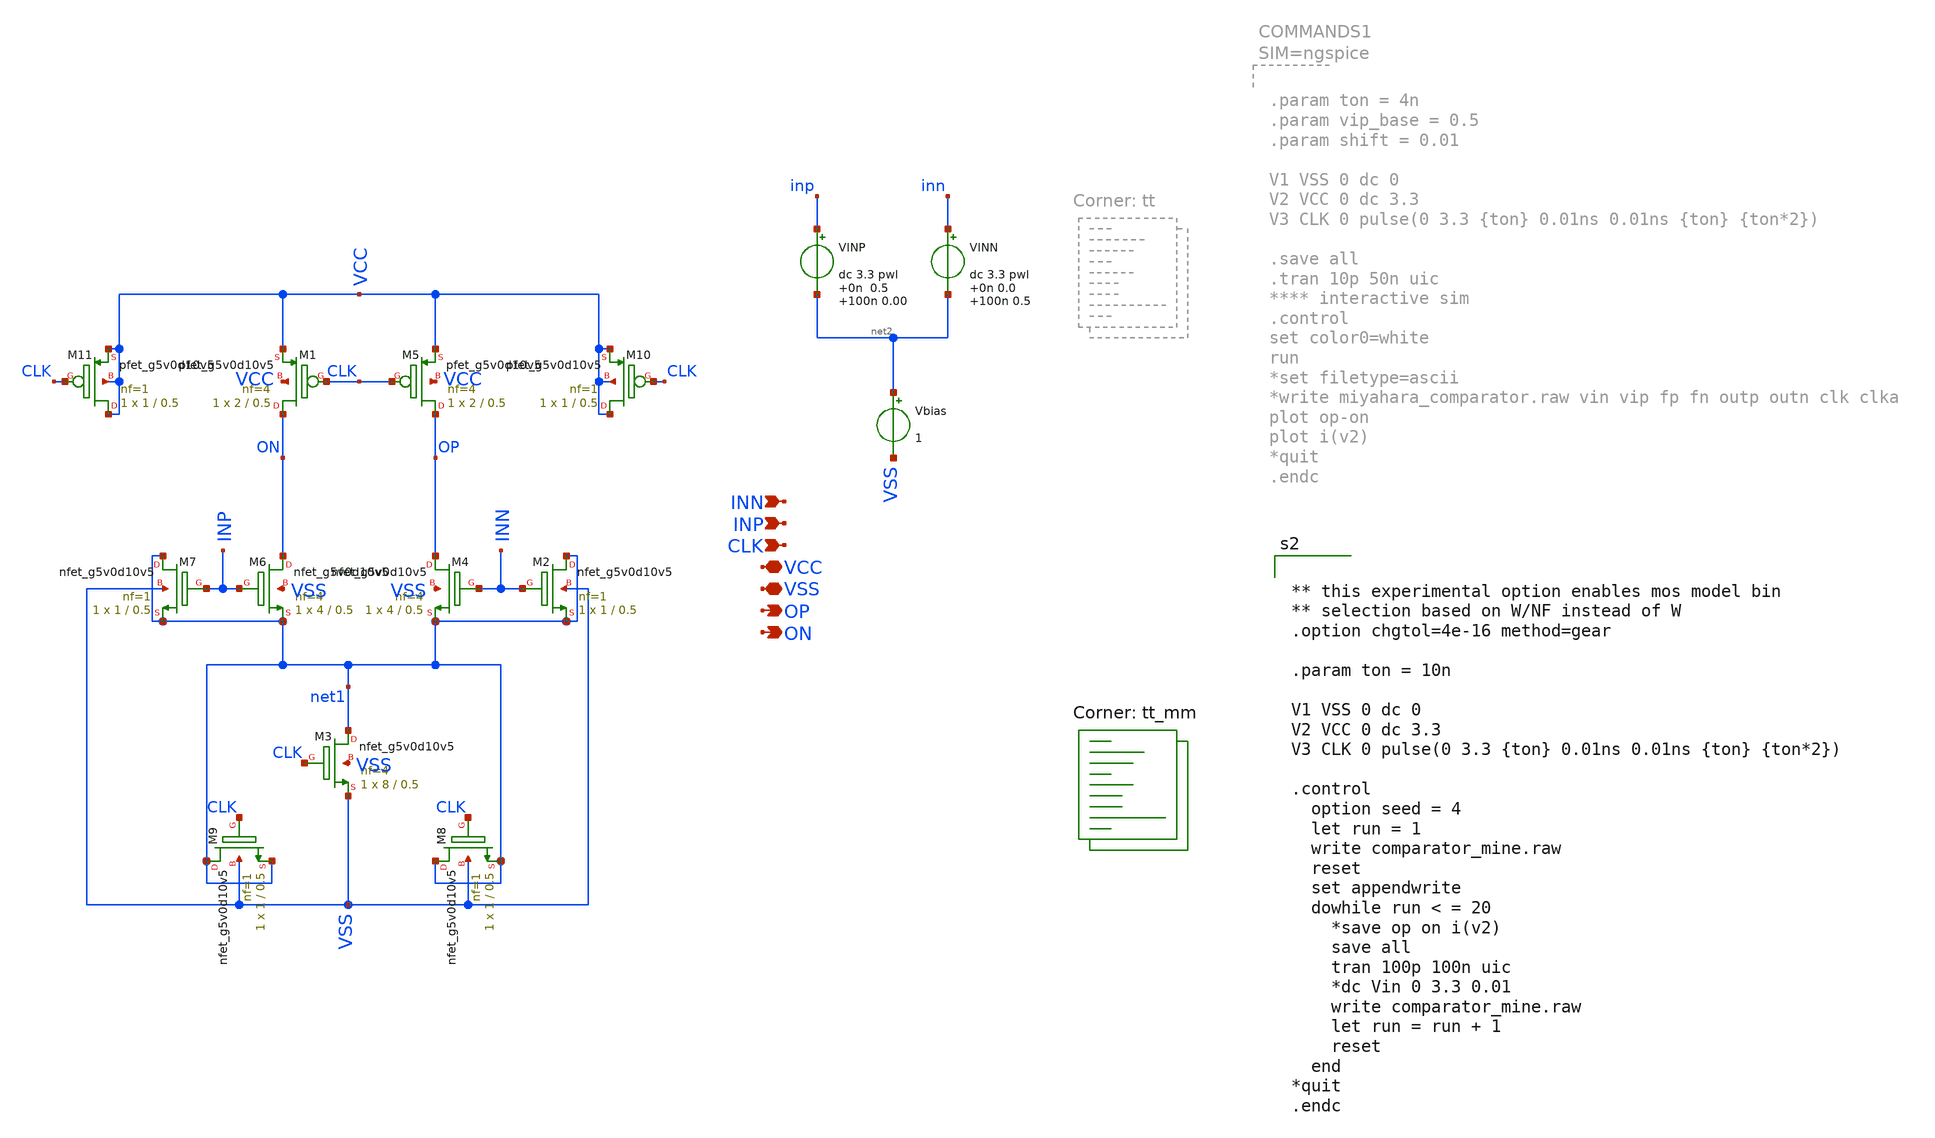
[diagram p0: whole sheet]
** sch_path: Comparator/schematic/new_comparator/comparator_mine.sch
**.subckt comparator_mine INP INN CLK VCC VSS OP ON
*.ipin INP
*.ipin INN
*.ipin CLK
*.iopin VCC
*.iopin VSS
*.opin OP
*.opin ON
VINP inp net2 dc 3.3 pwl 0n 0.5 100n 0.00
VINN inn net2 dc 3.3 pwl 0n 0.0 100n 0.5
Vbias net2 VSS 1
XM6 ON INP net1 VSS sky130_fd_pr__nfet_g5v0d10v5 L=0.5 W=4 nf=4 ad='int((nf+1)/2) * W/nf * 0.29' as='int((nf+2)/2) * W/nf * 0.29'
+ pd='2*int((nf+1)/2) * (W/nf + 0.29)' ps='2*int((nf+2)/2) * (W/nf + 0.29)' nrd='0.29 / W' nrs='0.29 / W'
+ sa=0 sb=0 sd=0 mult=1 m=1
XM4 OP INN net1 VSS sky130_fd_pr__nfet_g5v0d10v5 L=0.5 W=4 nf=4 ad='int((nf+1)/2) * W/nf * 0.29' as='int((nf+2)/2) * W/nf * 0.29'
+ pd='2*int((nf+1)/2) * (W/nf + 0.29)' ps='2*int((nf+2)/2) * (W/nf + 0.29)' nrd='0.29 / W' nrs='0.29 / W'
+ sa=0 sb=0 sd=0 mult=1 m=1
XM3 net1 CLK VSS VSS sky130_fd_pr__nfet_g5v0d10v5 L=0.5 W=8 nf=4 ad='int((nf+1)/2) * W/nf * 0.29' as='int((nf+2)/2) * W/nf * 0.29'
+ pd='2*int((nf+1)/2) * (W/nf + 0.29)' ps='2*int((nf+2)/2) * (W/nf + 0.29)' nrd='0.29 / W' nrs='0.29 / W'
+ sa=0 sb=0 sd=0 mult=1 m=1
XM5 OP CLK VCC VCC sky130_fd_pr__pfet_g5v0d10v5 L=0.5 W=2 nf=4 ad='int((nf+1)/2) * W/nf * 0.29' as='int((nf+2)/2) * W/nf * 0.29'
+ pd='2*int((nf+1)/2) * (W/nf + 0.29)' ps='2*int((nf+2)/2) * (W/nf + 0.29)' nrd='0.29 / W' nrs='0.29 / W'
+ sa=0 sb=0 sd=0 mult=1 m=1
XM1 ON CLK VCC VCC sky130_fd_pr__pfet_g5v0d10v5 L=0.5 W=2 nf=4 ad='int((nf+1)/2) * W/nf * 0.29' as='int((nf+2)/2) * W/nf * 0.29'
+ pd='2*int((nf+1)/2) * (W/nf + 0.29)' ps='2*int((nf+2)/2) * (W/nf + 0.29)' nrd='0.29 / W' nrs='0.29 / W'
+ sa=0 sb=0 sd=0 mult=1 m=1
XM2 net1 INN net1 VSS sky130_fd_pr__nfet_g5v0d10v5 L=0.5 W=1 nf=1 ad='int((nf+1)/2) * W/nf * 0.29' as='int((nf+2)/2) * W/nf * 0.29'
+ pd='2*int((nf+1)/2) * (W/nf + 0.29)' ps='2*int((nf+2)/2) * (W/nf + 0.29)' nrd='0.29 / W' nrs='0.29 / W'
+ sa=0 sb=0 sd=0 mult=1 m=1
XM7 net1 INP net1 VSS sky130_fd_pr__nfet_g5v0d10v5 L=0.5 W=1 nf=1 ad='int((nf+1)/2) * W/nf * 0.29' as='int((nf+2)/2) * W/nf * 0.29'
+ pd='2*int((nf+1)/2) * (W/nf + 0.29)' ps='2*int((nf+2)/2) * (W/nf + 0.29)' nrd='0.29 / W' nrs='0.29 / W'
+ sa=0 sb=0 sd=0 mult=1 m=1
XM9 net1 CLK net1 VSS sky130_fd_pr__nfet_g5v0d10v5 L=0.5 W=1 nf=1 ad='int((nf+1)/2) * W/nf * 0.29' as='int((nf+2)/2) * W/nf * 0.29'
+ pd='2*int((nf+1)/2) * (W/nf + 0.29)' ps='2*int((nf+2)/2) * (W/nf + 0.29)' nrd='0.29 / W' nrs='0.29 / W'
+ sa=0 sb=0 sd=0 mult=1 m=1
XM10 VCC CLK VCC VCC sky130_fd_pr__pfet_g5v0d10v5 L=0.5 W=1 nf=1 ad='int((nf+1)/2) * W/nf * 0.29' as='int((nf+2)/2) * W/nf * 0.29'
+ pd='2*int((nf+1)/2) * (W/nf + 0.29)' ps='2*int((nf+2)/2) * (W/nf + 0.29)' nrd='0.29 / W' nrs='0.29 / W'
+ sa=0 sb=0 sd=0 mult=1 m=1
XM11 VCC CLK VCC VCC sky130_fd_pr__pfet_g5v0d10v5 L=0.5 W=1 nf=1 ad='int((nf+1)/2) * W/nf * 0.29' as='int((nf+2)/2) * W/nf * 0.29'
+ pd='2*int((nf+1)/2) * (W/nf + 0.29)' ps='2*int((nf+2)/2) * (W/nf + 0.29)' nrd='0.29 / W' nrs='0.29 / W'
+ sa=0 sb=0 sd=0 mult=1 m=1
XM8 net1 CLK net1 VSS sky130_fd_pr__nfet_g5v0d10v5 L=0.5 W=1 nf=1 ad='int((nf+1)/2) * W/nf * 0.29' as='int((nf+2)/2) * W/nf * 0.29'
+ pd='2*int((nf+1)/2) * (W/nf + 0.29)' ps='2*int((nf+2)/2) * (W/nf + 0.29)' nrd='0.29 / W' nrs='0.29 / W'
+ sa=0 sb=0 sd=0 mult=1 m=1
**** begin user architecture code


** this experimental option enables mos model bin
** selection based on W/NF instead of W
.option chgtol=4e-16 method=gear

.param ton = 10n

V1 VSS 0 dc 0
V2 VCC 0 dc 3.3
V3 CLK 0 pulse(0 3.3 {ton} 0.01ns 0.01ns {ton} {ton*2})

.control
  option seed = 4
  let run = 1
  write comparator_mine.raw
  reset
  set appendwrite
  dowhile run < = 20
    *save op on i(v2)
    save all
    tran 100p 100n uic
    *dc Vin 0 3.3 0.01
    write comparator_mine.raw
    let run = run + 1
    reset
  end
*quit
.endc



.lib $::SKYWATER_MODELS/sky130.lib.spice tt_mm
**** end user architecture code
**.ends
.end
